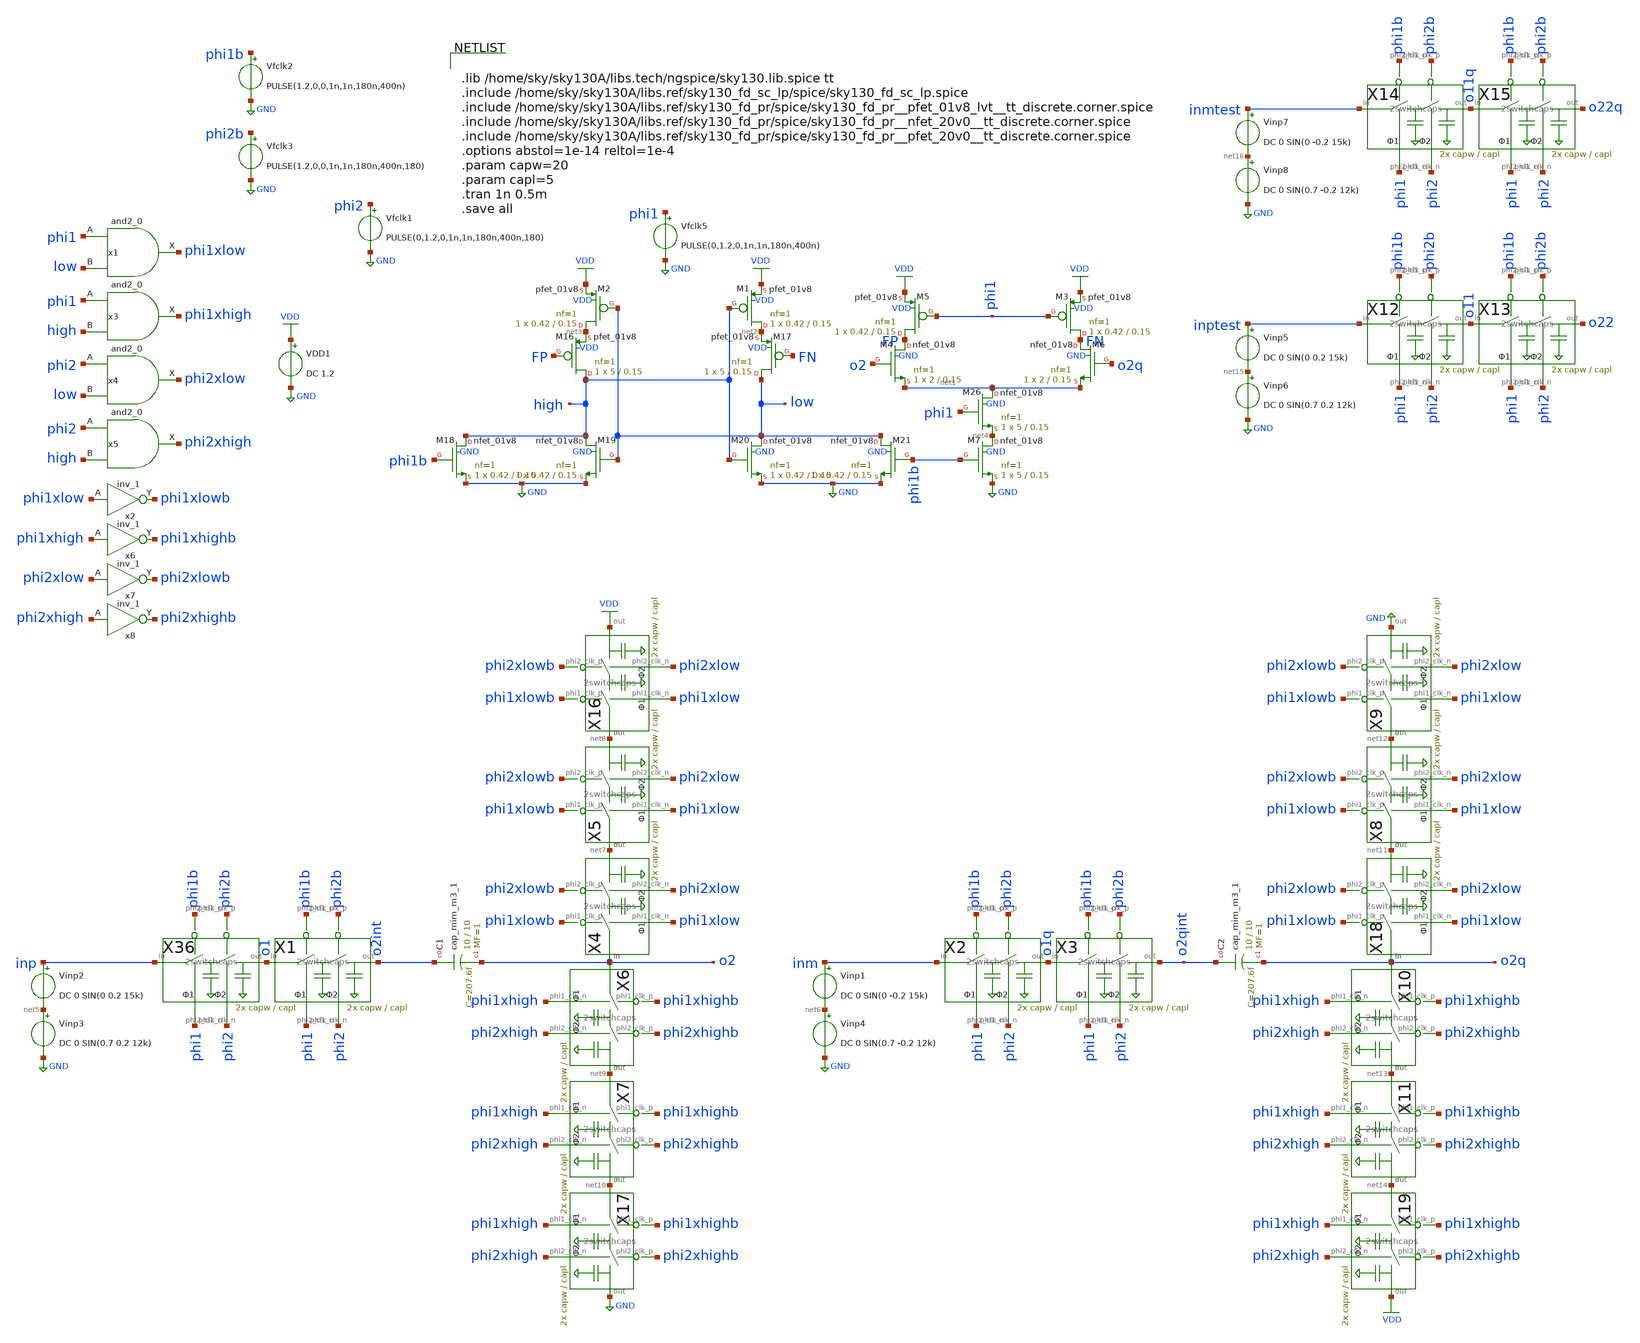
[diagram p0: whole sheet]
** sch_path: xschem/comparator_with_AZ/comp_with_AZ_TB.sch
**.subckt comp_with_AZ_TB
X36 inp o1 phi2 phi1 phi1b phi2b 2switchcaps Wcap=capw Lcap=capl
X1 o1 o2int phi2 phi1 phi1b phi2b 2switchcaps Wcap=capw Lcap=capl
VDD1 VDD GND DC 1.2
Vfclk5 phi1 GND PULSE(0,1.2,0,1n,1n,180n,400n)
XM1 net2 high VDD VDD sky130_fd_pr__pfet_01v8 L=0.15 W=0.42 nf=1 ad='int((nf+1)/2) * W/nf * 0.29' as='int((nf+2)/2) * W/nf * 0.29'
+ pd='2*int((nf+1)/2) * (W/nf + 0.29)' ps='2*int((nf+2)/2) * (W/nf + 0.29)' nrd='0.29 / W' nrs='0.29 / W'
+ sa=0 sb=0 sd=0 mult=1 m=1
XM2 net3 low VDD VDD sky130_fd_pr__pfet_01v8 L=0.15 W=0.42 nf=1 ad='int((nf+1)/2) * W/nf * 0.29' as='int((nf+2)/2) * W/nf * 0.29'
+ pd='2*int((nf+1)/2) * (W/nf + 0.29)' ps='2*int((nf+2)/2) * (W/nf + 0.29)' nrd='0.29 / W' nrs='0.29 / W'
+ sa=0 sb=0 sd=0 mult=1 m=1
XM16 high FP net3 VDD sky130_fd_pr__pfet_01v8 L=0.15 W=5 nf=1 ad='int((nf+1)/2) * W/nf * 0.29' as='int((nf+2)/2) * W/nf * 0.29'
+ pd='2*int((nf+1)/2) * (W/nf + 0.29)' ps='2*int((nf+2)/2) * (W/nf + 0.29)' nrd='0.29 / W' nrs='0.29 / W'
+ sa=0 sb=0 sd=0 mult=1 m=1
XM17 low FN net2 VDD sky130_fd_pr__pfet_01v8 L=0.15 W=5 nf=1 ad='int((nf+1)/2) * W/nf * 0.29' as='int((nf+2)/2) * W/nf * 0.29'
+ pd='2*int((nf+1)/2) * (W/nf + 0.29)' ps='2*int((nf+2)/2) * (W/nf + 0.29)' nrd='0.29 / W' nrs='0.29 / W'
+ sa=0 sb=0 sd=0 mult=1 m=1
XM18 high phi1b GND GND sky130_fd_pr__nfet_01v8 L=0.15 W=0.42 nf=1 ad='int((nf+1)/2) * W/nf * 0.29' as='int((nf+2)/2) * W/nf * 0.29'
+ pd='2*int((nf+1)/2) * (W/nf + 0.29)' ps='2*int((nf+2)/2) * (W/nf + 0.29)' nrd='0.29 / W' nrs='0.29 / W'
+ sa=0 sb=0 sd=0 mult=1 m=1
XM19 high low GND GND sky130_fd_pr__nfet_01v8 L=0.15 W=0.42 nf=1 ad='int((nf+1)/2) * W/nf * 0.29' as='int((nf+2)/2) * W/nf * 0.29'
+ pd='2*int((nf+1)/2) * (W/nf + 0.29)' ps='2*int((nf+2)/2) * (W/nf + 0.29)' nrd='0.29 / W' nrs='0.29 / W'
+ sa=0 sb=0 sd=0 mult=1 m=1
XM20 low high GND GND sky130_fd_pr__nfet_01v8 L=0.15 W=0.42 nf=1 ad='int((nf+1)/2) * W/nf * 0.29' as='int((nf+2)/2) * W/nf * 0.29'
+ pd='2*int((nf+1)/2) * (W/nf + 0.29)' ps='2*int((nf+2)/2) * (W/nf + 0.29)' nrd='0.29 / W' nrs='0.29 / W'
+ sa=0 sb=0 sd=0 mult=1 m=1
XM21 low phi1b GND GND sky130_fd_pr__nfet_01v8 L=0.15 W=0.42 nf=1 ad='int((nf+1)/2) * W/nf * 0.29' as='int((nf+2)/2) * W/nf * 0.29'
+ pd='2*int((nf+1)/2) * (W/nf + 0.29)' ps='2*int((nf+2)/2) * (W/nf + 0.29)' nrd='0.29 / W' nrs='0.29 / W'
+ sa=0 sb=0 sd=0 mult=1 m=1
XM26 net1 phi1 net4 GND sky130_fd_pr__nfet_01v8 L=0.15 W=5 nf=1 ad='int((nf+1)/2) * W/nf * 0.29' as='int((nf+2)/2) * W/nf * 0.29'
+ pd='2*int((nf+1)/2) * (W/nf + 0.29)' ps='2*int((nf+2)/2) * (W/nf + 0.29)' nrd='0.29 / W' nrs='0.29 / W'
+ sa=0 sb=0 sd=0 mult=1 m=1
Vfclk1 phi2 GND PULSE(0,1.2,0,1n,1n,180n,400n,180)
Vfclk2 phi1b GND PULSE(1.2,0,0,1n,1n,180n,400n)
Vfclk3 phi2b GND PULSE(1.2,0,0,1n,1n,180n,400n,180)
XM3 FN phi1 VDD VDD sky130_fd_pr__pfet_01v8 L=0.15 W=0.42 nf=1 ad='int((nf+1)/2) * W/nf * 0.29' as='int((nf+2)/2) * W/nf * 0.29'
+ pd='2*int((nf+1)/2) * (W/nf + 0.29)' ps='2*int((nf+2)/2) * (W/nf + 0.29)' nrd='0.29 / W' nrs='0.29 / W'
+ sa=0 sb=0 sd=0 mult=1 m=1
XM5 FP phi1 VDD VDD sky130_fd_pr__pfet_01v8 L=0.15 W=0.42 nf=1 ad='int((nf+1)/2) * W/nf * 0.29' as='int((nf+2)/2) * W/nf * 0.29'
+ pd='2*int((nf+1)/2) * (W/nf + 0.29)' ps='2*int((nf+2)/2) * (W/nf + 0.29)' nrd='0.29 / W' nrs='0.29 / W'
+ sa=0 sb=0 sd=0 mult=1 m=1
Vinp2 inp net5 DC 0 SIN(0 0.2 15k)
Vinp3 net5 GND DC 0 SIN(0.7 0.2 12k)
X2 inm o1q phi2 phi1 phi1b phi2b 2switchcaps Wcap=capw Lcap=capl
X3 o1q o2qint phi2 phi1 phi1b phi2b 2switchcaps Wcap=capw Lcap=capl
Vinp1 inm net6 DC 0 SIN(0 -0.2 15k)
Vinp4 net6 GND DC 0 SIN(0.7 -0.2 12k)
XC1 o2int o2 sky130_fd_pr__cap_mim_m3_1 W=10 L=10 MF=1 m=1
X4 o2 net7 phi2xlow phi1xlow phi1xlowb phi2xlowb 2switchcaps Wcap=capw Lcap=capl
X5 net7 net8 phi2xlow phi1xlow phi1xlowb phi2xlowb 2switchcaps Wcap=capw Lcap=capl
X6 o2 net9 phi2xhigh phi1xhigh phi1xhighb phi2xhighb 2switchcaps Wcap=capw Lcap=capl
X7 net9 net10 phi2xhigh phi1xhigh phi1xhighb phi2xhighb 2switchcaps Wcap=capw Lcap=capl
x1 phi1 low GND GND VDD VDD phi1xlow sky130_fd_sc_lp__and2_0
x2 phi1xlow GND GND VDD VDD phi1xlowb sky130_fd_sc_lp__inv_1
x3 phi1 high GND GND VDD VDD phi1xhigh sky130_fd_sc_lp__and2_0
x4 phi2 low GND GND VDD VDD phi2xlow sky130_fd_sc_lp__and2_0
x5 phi2 high GND GND VDD VDD phi2xhigh sky130_fd_sc_lp__and2_0
x6 phi1xhigh GND GND VDD VDD phi1xhighb sky130_fd_sc_lp__inv_1
x7 phi2xlow GND GND VDD VDD phi2xlowb sky130_fd_sc_lp__inv_1
x8 phi2xhigh GND GND VDD VDD phi2xhighb sky130_fd_sc_lp__inv_1
XC2 o2qint o2q sky130_fd_pr__cap_mim_m3_1 W=10 L=10 MF=1 m=1
X8 net11 net12 phi2xlow phi1xlow phi1xlowb phi2xlowb 2switchcaps Wcap=capw Lcap=capl
X9 net12 GND phi2xlow phi1xlow phi1xlowb phi2xlowb 2switchcaps Wcap=capw Lcap=capl
X10 o2q net13 phi2xhigh phi1xhigh phi1xhighb phi2xhighb 2switchcaps Wcap=capw Lcap=capl
X11 net13 net14 phi2xhigh phi1xhigh phi1xhighb phi2xhighb 2switchcaps Wcap=capw Lcap=capl
X12 inptest o11 phi2 phi1 phi1b phi2b 2switchcaps Wcap=capw Lcap=capl
X13 o11 o22 phi2 phi1 phi1b phi2b 2switchcaps Wcap=capw Lcap=capl
Vinp5 inptest net15 DC 0 SIN(0 0.2 15k)
Vinp6 net15 GND DC 0 SIN(0.7 0.2 12k)
X14 inmtest o11q phi2 phi1 phi1b phi2b 2switchcaps Wcap=capw Lcap=capl
X15 o11q o22q phi2 phi1 phi1b phi2b 2switchcaps Wcap=capw Lcap=capl
Vinp7 inmtest net16 DC 0 SIN(0 -0.2 15k)
Vinp8 net16 GND DC 0 SIN(0.7 -0.2 12k)
XM4 FP o2 net1 GND sky130_fd_pr__nfet_01v8 L=0.15 W=2 nf=1 ad='int((nf+1)/2) * W/nf * 0.29' as='int((nf+2)/2) * W/nf * 0.29'
+ pd='2*int((nf+1)/2) * (W/nf + 0.29)' ps='2*int((nf+2)/2) * (W/nf + 0.29)' nrd='0.29 / W' nrs='0.29 / W'
+ sa=0 sb=0 sd=0 mult=1 m=1
XM6 FN o2q net1 GND sky130_fd_pr__nfet_01v8 L=0.15 W=2 nf=1 ad='int((nf+1)/2) * W/nf * 0.29' as='int((nf+2)/2) * W/nf * 0.29'
+ pd='2*int((nf+1)/2) * (W/nf + 0.29)' ps='2*int((nf+2)/2) * (W/nf + 0.29)' nrd='0.29 / W' nrs='0.29 / W'
+ sa=0 sb=0 sd=0 mult=1 m=1
XM7 net4 phi1b GND GND sky130_fd_pr__nfet_01v8 L=0.15 W=5 nf=1 ad='int((nf+1)/2) * W/nf * 0.29' as='int((nf+2)/2) * W/nf * 0.29'
+ pd='2*int((nf+1)/2) * (W/nf + 0.29)' ps='2*int((nf+2)/2) * (W/nf + 0.29)' nrd='0.29 / W' nrs='0.29 / W'
+ sa=0 sb=0 sd=0 mult=1 m=1
X16 net8 VDD phi2xlow phi1xlow phi1xlowb phi2xlowb 2switchcaps Wcap=capw Lcap=capl
X17 net10 GND phi2xhigh phi1xhigh phi1xhighb phi2xhighb 2switchcaps Wcap=capw Lcap=capl
X18 o2q net11 phi2xlow phi1xlow phi1xlowb phi2xlowb 2switchcaps Wcap=capw Lcap=capl
X19 net14 VDD phi2xhigh phi1xhigh phi1xhighb phi2xhighb 2switchcaps Wcap=capw Lcap=capl
**** begin user architecture code


.lib /home/sky/sky130A/libs.tech/ngspice/sky130.lib.spice tt
.include /home/sky/sky130A/libs.ref/sky130_fd_sc_lp/spice/sky130_fd_sc_lp.spice
.include /home/sky/sky130A/libs.ref/sky130_fd_pr/spice/sky130_fd_pr__pfet_01v8_lvt__tt_discrete.corner.spice
.include /home/sky/sky130A/libs.ref/sky130_fd_pr/spice/sky130_fd_pr__nfet_20v0__tt_discrete.corner.spice
.include /home/sky/sky130A/libs.ref/sky130_fd_pr/spice/sky130_fd_pr__pfet_20v0__tt_discrete.corner.spice
.options abstol=1e-14 reltol=1e-4
.param capw=20
.param capl=5
.tran 1n 0.5m
.save all


**** end user architecture code
**.ends

* expanding   symbol:  comparator_with_AZ/2switchcaps.sym # of pins=6
** sym_path: xschem/comparator_with_AZ/2switchcaps.sym
** sch_path: xschem/comparator_with_AZ/2switchcaps.sch
.subckt 2switchcaps in out phi2_clk_n phi1_clk_n phi1_clk_p phi2_clk_p  Wcap=20 Lcap=20
*.iopin out
*.iopin in
*.ipin phi1_clk_n
*.ipin phi1_clk_p
*.ipin phi2_clk_p
*.ipin phi2_clk_n
XC1 c1 GND sky130_fd_pr__cap_mim_m3_1 W=3 L=3 MF=1 m=1
XC2 out GND sky130_fd_pr__cap_mim_m3_1 W=Wcap L=Lcap MF=1 m=1
**** begin user architecture code

.ic v(c1)=0 v(out)=0

**** end user architecture code
X1 in c1 phi1_clk_p phi1_clk_n transmission_gate Wpmos=0.42 Lpmos=0.15 Wnmos=0.42 Lnmos=0.15
X2 c1 out phi2_clk_p phi2_clk_n transmission_gate Wpmos=0.42 Lpmos=0.15 Wnmos=0.42 Lnmos=0.15
.ends


* expanding   symbol:  transmission_gate/transmission_gate.sym # of pins=4
** sym_path: xschem/transmission_gate/transmission_gate.sym
** sch_path: xschem/transmission_gate/transmission_gate.sch
.subckt transmission_gate in out ctrl_ ctrl  Wpmos=0.42 Lpmos=0.18 Wnmos=0.42 Lnmos=0.18
*.iopin in
*.iopin out
*.ipin ctrl_
*.ipin ctrl
XM1 out ctrl in GND sky130_fd_pr__nfet_01v8 L=Lnmos W=Wnmos nf=1 ad='int((nf+1)/2) * W/nf * 0.29' as='int((nf+2)/2) * W/nf * 0.29'
+ pd='2*int((nf+1)/2) * (W/nf + 0.29)' ps='2*int((nf+2)/2) * (W/nf + 0.29)' nrd='0.29 / W' nrs='0.29 / W'
+ sa=0 sb=0 sd=0 mult=1 m=1
XM2 out ctrl_ in VDD sky130_fd_pr__pfet_01v8 L=Lpmos W=Wpmos nf=1 ad='int((nf+1)/2) * W/nf * 0.29' as='int((nf+2)/2) * W/nf * 0.29'
+ pd='2*int((nf+1)/2) * (W/nf + 0.29)' ps='2*int((nf+2)/2) * (W/nf + 0.29)' nrd='0.29 / W' nrs='0.29 / W'
+ sa=0 sb=0 sd=0 mult=1 m=1
.ends

.GLOBAL GND
.GLOBAL VDD
.end
